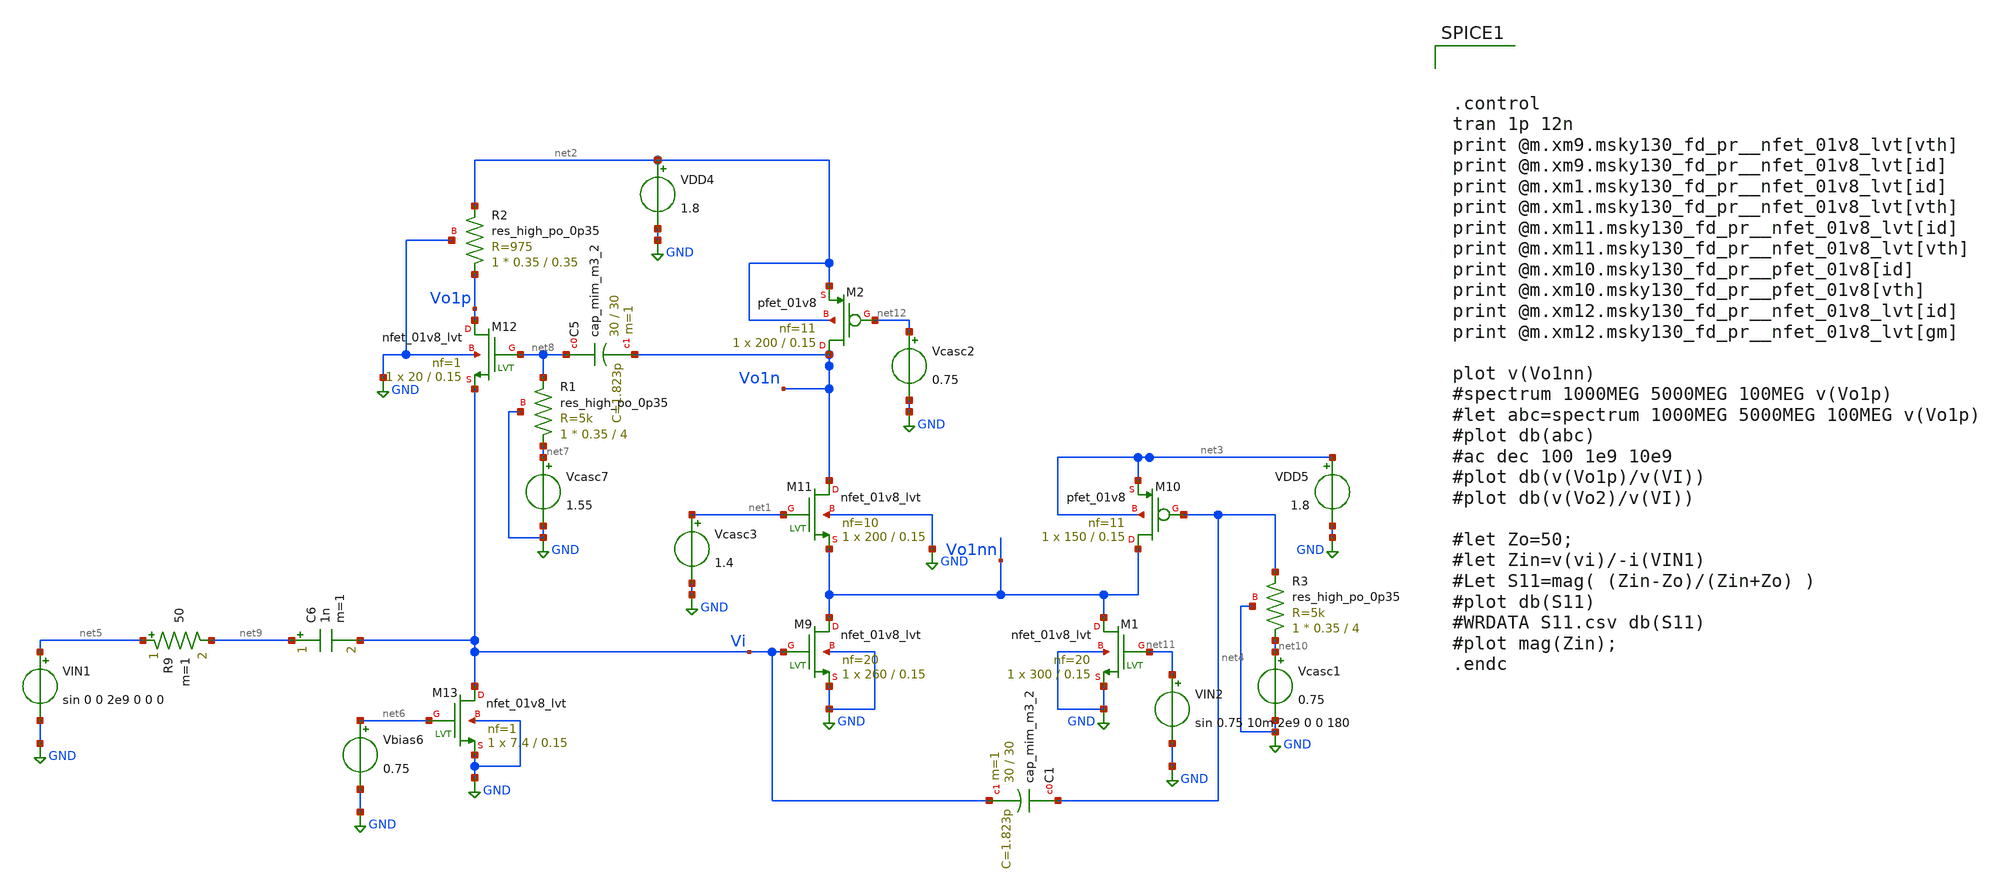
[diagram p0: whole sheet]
** sch_path: xschem/xschem4_sic_final/Com_amp_tran.sch
**.subckt Com_amp_tran
VIN1 net5 GND sin 0 0 2e9 0 0 0
Vcasc3 net1 GND 1.4
VDD4 net2 GND 1.8
VDD5 net3 GND 1.8
Vbias6 net6 GND 0.75
Vcasc7 net7 GND 1.55
XR1 net7 net8 GND sky130_fd_pr__res_high_po_0p35 L=4 mult=1 m=1
XC5 net8 Vo1n sky130_fd_pr__cap_mim_m3_2 W=30 L=30 MF=1 m=1
C6 net9 Vi 1n m=1
XM9 Vo1nn Vi GND GND sky130_fd_pr__nfet_01v8_lvt L=0.15 W=260 nf=20 ad='int((nf+1)/2) * W/nf * 0.29'
+ as='int((nf+2)/2) * W/nf * 0.29' pd='2*int((nf+1)/2) * (W/nf + 0.29)' ps='2*int((nf+2)/2) * (W/nf + 0.29)'
+ nrd='0.29 / W' nrs='0.29 / W' sa=0 sb=0 sd=0 mult=1 m=1
XM10 Vo1nn net4 net3 net3 sky130_fd_pr__pfet_01v8 L=0.15 W=150 nf=11 ad='int((nf+1)/2) * W/nf * 0.29'
+ as='int((nf+2)/2) * W/nf * 0.29' pd='2*int((nf+1)/2) * (W/nf + 0.29)' ps='2*int((nf+2)/2) * (W/nf + 0.29)'
+ nrd='0.29 / W' nrs='0.29 / W' sa=0 sb=0 sd=0 mult=1 m=1
XM11 Vo1n net1 Vo1nn GND sky130_fd_pr__nfet_01v8_lvt L=0.15 W=200 nf=10 ad='int((nf+1)/2) * W/nf * 0.29'
+ as='int((nf+2)/2) * W/nf * 0.29' pd='2*int((nf+1)/2) * (W/nf + 0.29)' ps='2*int((nf+2)/2) * (W/nf + 0.29)'
+ nrd='0.29 / W' nrs='0.29 / W' sa=0 sb=0 sd=0 mult=1 m=1
XM12 Vo1p net8 Vi GND sky130_fd_pr__nfet_01v8_lvt L=0.15 W=20 nf=1 ad='int((nf+1)/2) * W/nf * 0.29' as='int((nf+2)/2) * W/nf * 0.29'
+ pd='2*int((nf+1)/2) * (W/nf + 0.29)' ps='2*int((nf+2)/2) * (W/nf + 0.29)' nrd='0.29 / W' nrs='0.29 / W'
+ sa=0 sb=0 sd=0 mult=1 m=1
XM13 Vi net6 GND GND sky130_fd_pr__nfet_01v8_lvt L=0.15 W=7.4 nf=1 ad='int((nf+1)/2) * W/nf * 0.29' as='int((nf+2)/2) * W/nf * 0.29'
+ pd='2*int((nf+1)/2) * (W/nf + 0.29)' ps='2*int((nf+2)/2) * (W/nf + 0.29)' nrd='0.29 / W' nrs='0.29 / W'
+ sa=0 sb=0 sd=0 mult=1 m=1
R9 net5 net9 50 m=1
XC1 net4 Vi sky130_fd_pr__cap_mim_m3_2 W=30 L=30 MF=1 m=1
Vcasc1 net10 GND 0.75
XR3 net10 net4 GND sky130_fd_pr__res_high_po_0p35 L=4 mult=1 m=1
XR2 Vo1p net2 GND sky130_fd_pr__res_high_po_0p35 L=0.35 mult=1 m=1
XM1 Vo1nn net11 GND GND sky130_fd_pr__nfet_01v8_lvt L=0.15 W=300 nf=20 ad='int((nf+1)/2) * W/nf * 0.29'
+ as='int((nf+2)/2) * W/nf * 0.29' pd='2*int((nf+1)/2) * (W/nf + 0.29)' ps='2*int((nf+2)/2) * (W/nf + 0.29)'
+ nrd='0.29 / W' nrs='0.29 / W' sa=0 sb=0 sd=0 mult=1 m=1
VIN2 net11 GND sin 0.75 10m 2e9 0 0 180
XM2 Vo1n net12 net2 net2 sky130_fd_pr__pfet_01v8 L=0.15 W=200 nf=11 ad='int((nf+1)/2) * W/nf * 0.29'
+ as='int((nf+2)/2) * W/nf * 0.29' pd='2*int((nf+1)/2) * (W/nf + 0.29)' ps='2*int((nf+2)/2) * (W/nf + 0.29)'
+ nrd='0.29 / W' nrs='0.29 / W' sa=0 sb=0 sd=0 mult=1 m=1
Vcasc2 net12 GND 0.75
**** begin user architecture code

.lib $::SKYWATER_MODELS/sky130.lib.spice tt




.control
tran 1p 12n
print @m.xm9.msky130_fd_pr__nfet_01v8_lvt[vth]
print @m.xm9.msky130_fd_pr__nfet_01v8_lvt[id]
print @m.xm1.msky130_fd_pr__nfet_01v8_lvt[id]
print @m.xm1.msky130_fd_pr__nfet_01v8_lvt[vth]
print @m.xm11.msky130_fd_pr__nfet_01v8_lvt[id]
print @m.xm11.msky130_fd_pr__nfet_01v8_lvt[vth]
print @m.xm10.msky130_fd_pr__pfet_01v8[id]
print @m.xm10.msky130_fd_pr__pfet_01v8[vth]
print @m.xm12.msky130_fd_pr__nfet_01v8_lvt[id]
print @m.xm12.msky130_fd_pr__nfet_01v8_lvt[gm]

plot v(Vo1nn)
#spectrum 1000MEG 5000MEG 100MEG v(Vo1p)
#let abc=spectrum 1000MEG 5000MEG 100MEG v(Vo1p)
#plot db(abc)
#ac dec 100 1e9 10e9
#plot db(v(Vo1p)/v(VI))
#plot db(v(Vo2)/v(VI))

#let Zo=50;
#let Zin=v(vi)/-i(VIN1)
#Let S11=mag( (Zin-Zo)/(Zin+Zo) )
#plot db(S11)
#WRDATA S11.csv db(S11)
#plot mag(Zin);
.endc


**** end user architecture code
**.ends
.GLOBAL GND
.end
